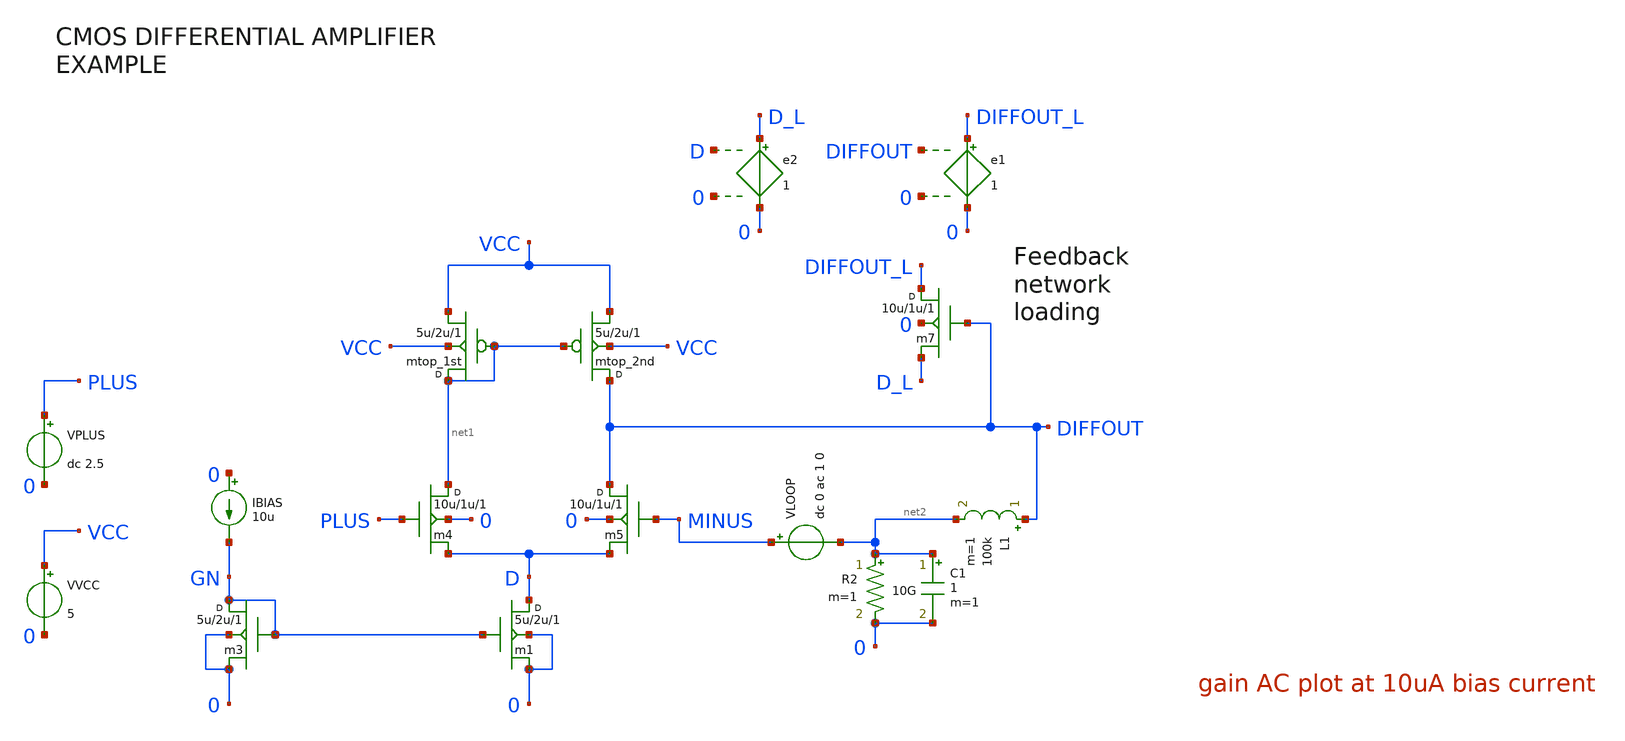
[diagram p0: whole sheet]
** sch_path: tests/test_sweep_diff/examples/test_ac_xyce/schematic/test_ac_xyce.sch
* Copyright (C) 1998-2024 Stefan Frederik Schippers
* This program is free software; you can redistribute it and/or modify
* it under the terms of the GNU General Public License as published by
* the Free Software Foundation; either version 2 of the License, or
* (at your option) any later version.
* This program is distributed in the hope that it will be useful,
* but WITHOUT ANY WARRANTY; without even the implied warranty of
* MERCHANTABILITY or FITNESS FOR A PARTICULAR PURPOSE.  See the
* GNU General Public License for more details.
* You should have received a copy of the GNU General Public License
* along with this program; if not, write to the Free Software
**.subckt test_ac_xyce
m1 D GN 0 0 cmosn w=5u l=2u m=1
mtop_2nd DIFFOUT net1 VCC VCC cmosp w=5u l=2u m=1
VVCC VCC 0 5
m3 GN GN 0 0 cmosn w=5u l=2u m=1
IBIAS 0 GN 10u
m4 net1 PLUS D 0 cmosn w=10u l=1u m=1
m5 DIFFOUT MINUS D 0 cmosn w=10u l=1u m=1
mtop_1st net1 net1 VCC VCC cmosp w=5u l=2u m=1
VPLUS PLUS 0 dc 2.5
e1 DIFFOUT_L 0 DIFFOUT 0 1
e2 D_L 0 D 0 1
m7 DIFFOUT_L DIFFOUT D_L 0 cmosn w=10u l=1u m=1
VLOOP MINUS net2 dc 0 ac 1 0
R2 net2 0 10G m=1
L1 DIFFOUT net2 100k m=1
C1 net2 0 1 m=1
**** begin user architecture code




** models are generally not free: you must download
** SPICE models for active devices and put them  into the below
** referenced file in netlist/simulation directory.
** http://bwrcs.eecs.berkeley.edu/Classes/icdesign/ee241_s00/ASSIGNMENTS/TSMC035-n96g-params.txt
.include "models_cmos_example.txt"

.control
.ac dec 10 1000 10G

** ngspice
* .save all

** xyce, not needed if -r given om cmdline
* .print tran format=raw v(diffout) v(plus) v(minus)


**** end user architecture code
**.ends
.end
